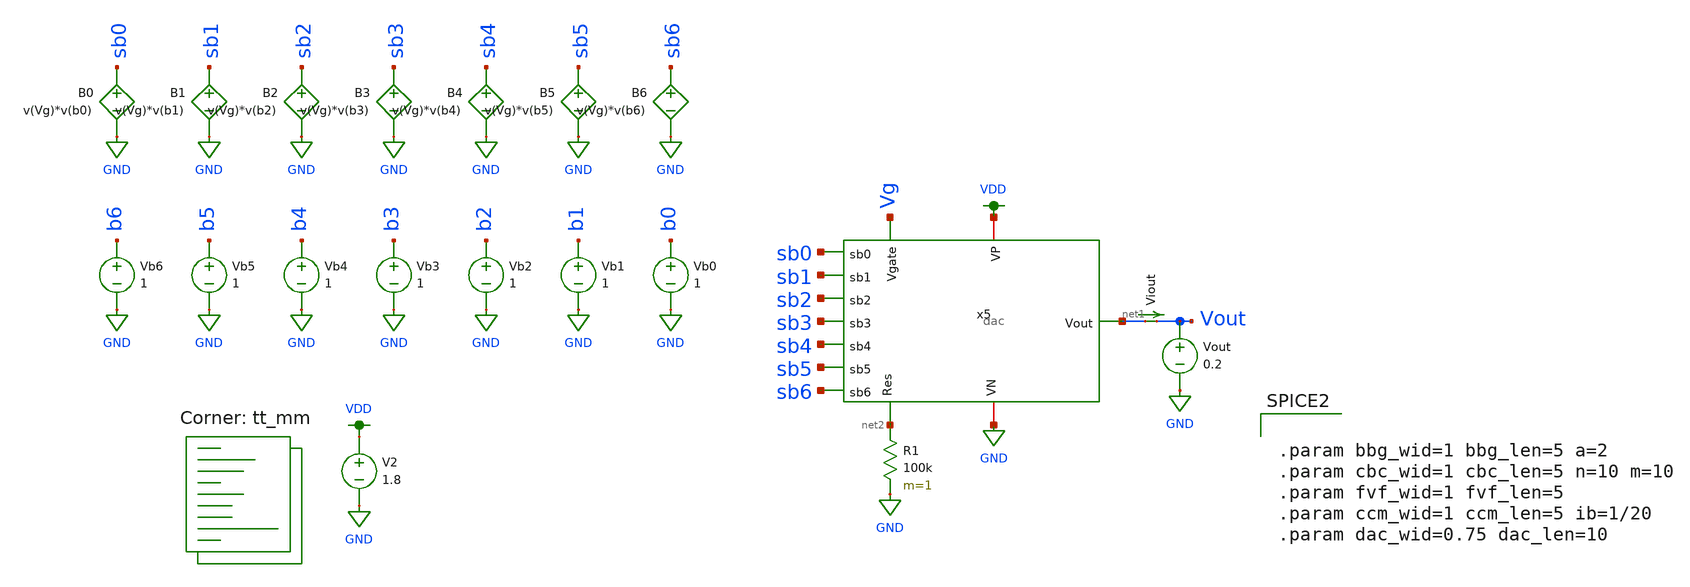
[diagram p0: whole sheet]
** sch_path: test_dac.sch
**.subckt test_dac
V2 VDD GND 1.8
R1 net2 GND 100k m=1
Vout Vout GND 0.2
Viout net1 Vout 0
.save i(viout)
Vb0 b0 GND 1
B0 sb0 GND V=v(Vg)*v(b0)
Vb1 b1 GND 1
B1 sb1 GND V=v(Vg)*v(b1)
Vb2 b2 GND 1
B2 sb2 GND V=v(Vg)*v(b2)
Vb3 b3 GND 1
B3 sb3 GND V=v(Vg)*v(b3)
Vb4 b4 GND 1
B4 sb4 GND V=v(Vg)*v(b4)
Vb5 b5 GND 1
B5 sb5 GND V=v(Vg)*v(b5)
Vb6 b6 GND 1
B6 sb6 GND V=v(Vg)*v(b6)
x5 VDD sb0 sb1 GND sb2 net1 Vg sb3 sb4 sb5 sb6 net2 dac
**** begin user architecture code
.lib $::SKYWATER_MODELS/sky130.lib.spice tt_mm


.control
  set wr_vecnames
  set wr_singlescale
  let mc_runs = 10
  let run = 1
  dowhile run <= mc_runs
    let code = 0
    while code < 128
      if code eq 0
        let b0 = 0
      else
        let b0 = code % 2
      end
      if floor(code / 2) eq 0
        let b1 = 0
      else
        let b1 = floor(code / 2) % 2
      end
      if floor(code / 4) eq 0
        let b2 = 0
      else
        let b2 = floor(code / 4) % 2
      end
      if floor(code / 8) eq 0
        let b3 = 0
      else
        let b3 = floor(code / 8) % 2
      end
      if floor(code / 16) eq 0
        let b4 = 0
      else
        let b4 = floor(code / 16) % 2
      end
      if floor(code / 32) eq 0
        let b5 = 0
      else
        let b5 = floor(code / 32) % 2
      end
      if floor(code / 64) eq 0
        let b6 = 0
      else
        let b6 = floor(code / 64) % 2
      end
      alter vb0 $&b0
      alter vb1 $&b1
      alter vb2 $&b2
      alter vb3 $&b3
      alter vb4 $&b4
      alter vb5 $&b5
      alter vb6 $&b6
      save all
      op
      wrdata ~/Documents/mosfet-dac/test_dac{$&run}.txt code v(sb0) v(sb1) v(sb2) v(sb3) v(sb4) v(sb5)
+ v(sb6) i(Viout) v(Vout)
      if code eq 0
        set appendwrite
        set wr_vecnames = FALSE
      end
      let code = code + 1
    end
    reset
    let run = run + 1
  end
quit
.endc



.param bbg_wid=1 bbg_len=5 a=2
.param cbc_wid=1 cbc_len=5 n=10 m=10
.param fvf_wid=1 fvf_len=5
.param ccm_wid=1 ccm_len=5 ib=1/20
.param dac_wid=0.75 dac_len=10


**** end user architecture code
**.ends
.GLOBAL GND
.GLOBAL VDD
.end
